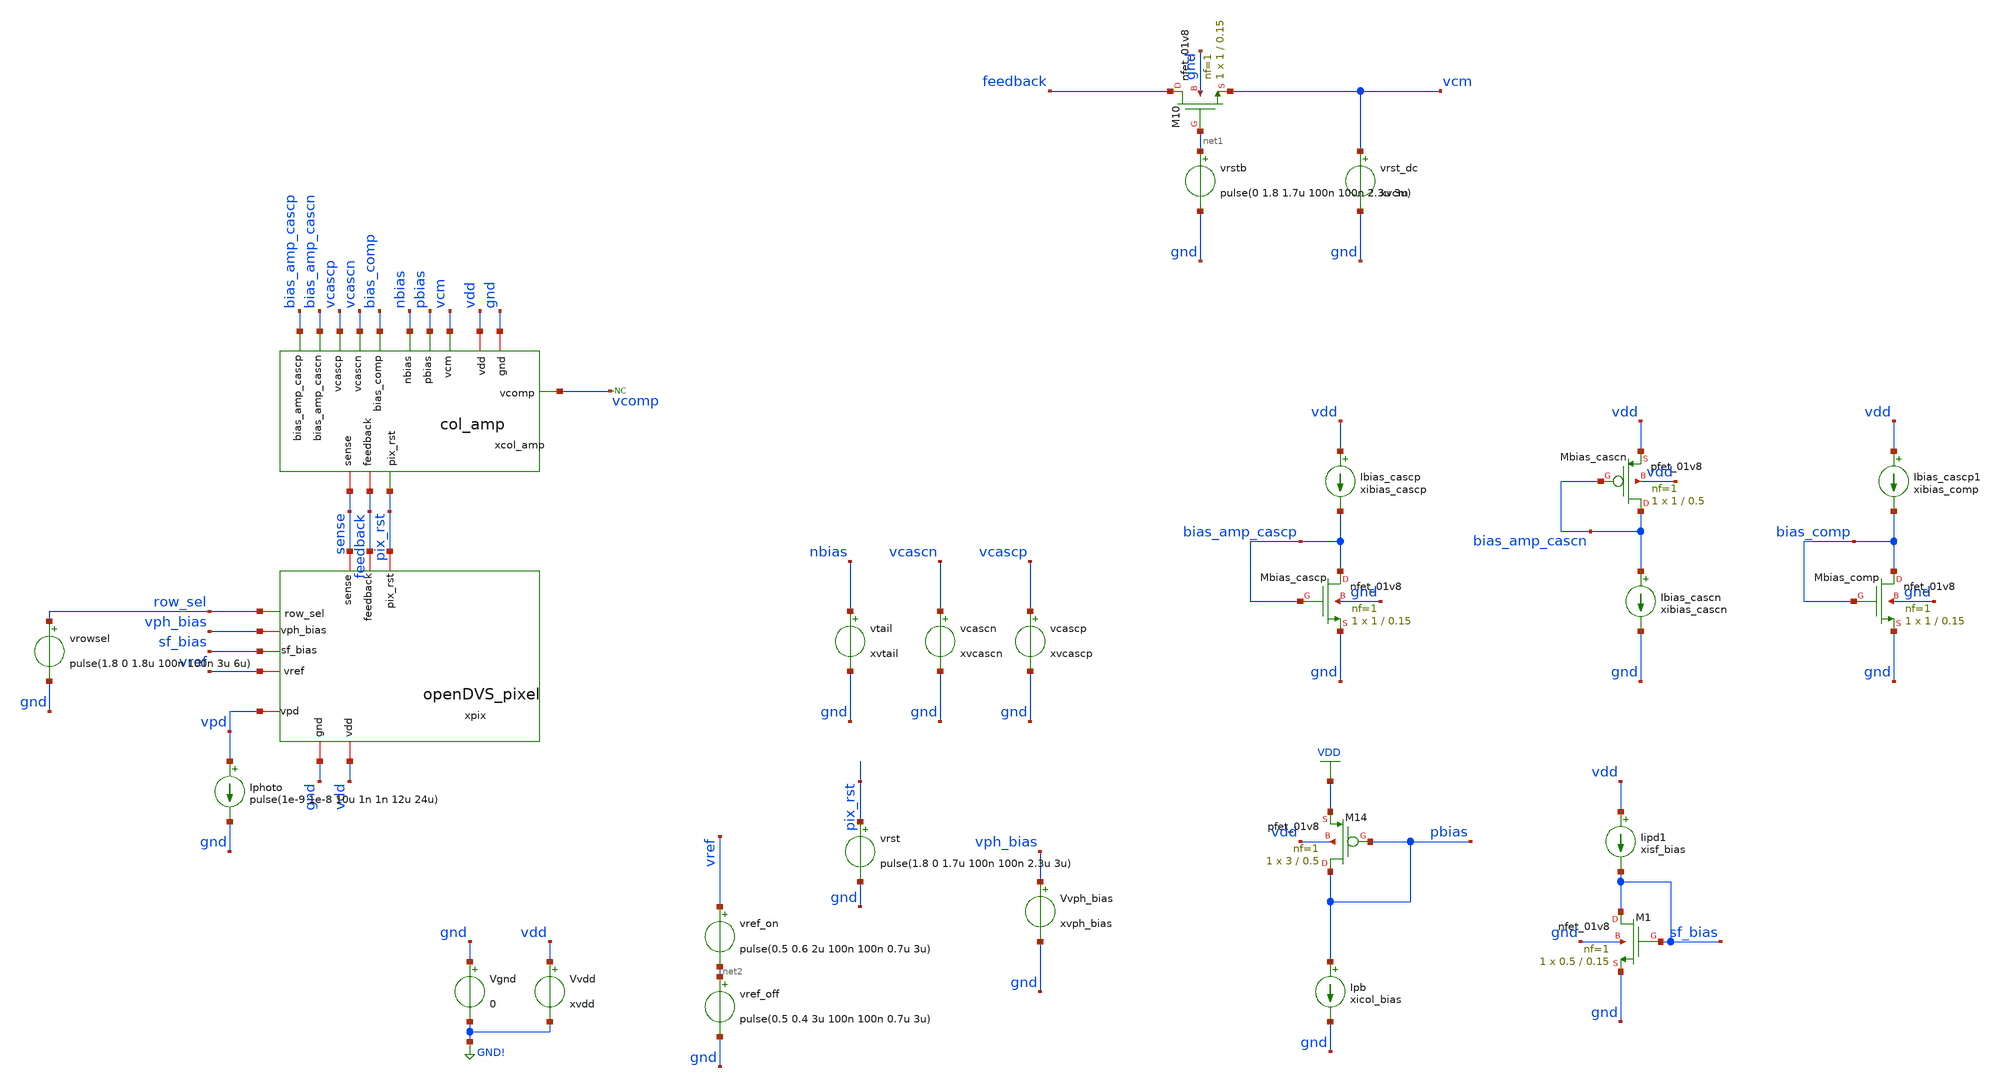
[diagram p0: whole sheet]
** sch_path: analog/xschem/1x1array_tb.sch
**.subckt 1x1array_tb
Ipb pbias gnd xicol_bias
XM14 pbias pbias VDD vdd sky130_fd_pr__pfet_01v8 L=0.5 W=3 nf=1 ad='int((1 + 1)/2) * 3 / 1 * 0.29' as='int((1 + 2)/2) * 3 / 1 * 0.29'
+ pd='2*int((1 + 1)/2) * (3 / 1 + 0.29)' ps='2*int((1 + 2)/2) * (3 / 1 + 0.29)' nrd='0.29 / 3 ' nrs='0.29 / 3 '
+ sa=0 sb=0 sd=0 mult=1 m=1
xcol_amp vdd pbias vcascp bias_amp_cascn vcm vcomp vcascn bias_comp pix_rst bias_amp_cascp gnd
+ feedback sense nbias col_amp
xpix feedback pix_rst sense row_sel vdd sf_bias gnd vref vpd vph_bias openDVS_pixel
XM1 sf_bias sf_bias gnd gnd sky130_fd_pr__nfet_01v8 L=0.15 W=0.5 nf=1 ad='int((1 + 1)/2) * 0.5 / 1 * 0.29'
+ as='int((1 + 2)/2) * 0.5 / 1 * 0.29' pd='2*int((1 + 1)/2) * (0.5 / 1 + 0.29)' ps='2*int((1 + 2)/2) * (0.5 / 1 + 0.29)'
+ nrd='0.29 / 0.5 ' nrs='0.29 / 0.5 ' sa=0 sb=0 sd=0 mult=1 m=1
Iipd1 vdd sf_bias xisf_bias
Vvph_bias vph_bias gnd xvph_bias
Vgnd gnd GND! 0
Vvdd vdd GND! xvdd
vtail nbias gnd xvtail
vcascn vcascn gnd xvcascn
vcascp vcascp gnd xvcascp
XMbias_cascp bias_amp_cascp bias_amp_cascp gnd gnd sky130_fd_pr__nfet_01v8 L=0.15 W=1 nf=1 ad='int((1 + 1)/2) * 1 / 1 * 0.29'
+ as='int((1 + 2)/2) * 1 / 1 * 0.29' pd='2*int((1 + 1)/2) * (1 / 1 + 0.29)' ps='2*int((1 + 2)/2) * (1 / 1 + 0.29)'
+ nrd='0.29 / 1 ' nrs='0.29 / 1 ' sa=0 sb=0 sd=0 mult=1 m=1
Ibias_cascp vdd bias_amp_cascp xibias_cascp
XMbias_cascn bias_amp_cascn bias_amp_cascn vdd vdd sky130_fd_pr__pfet_01v8 L=0.5 W=1 nf=1 ad='int((1 + 1)/2) * 1 / 1 * 0.29'
+ as='int((1 + 2)/2) * 1 / 1 * 0.29' pd='2*int((1 + 1)/2) * (1 / 1 + 0.29)' ps='2*int((1 + 2)/2) * (1 / 1 + 0.29)'
+ nrd='0.29 / 1 ' nrs='0.29 / 1 ' sa=0 sb=0 sd=0 mult=1 m=1
Ibias_cascn bias_amp_cascn gnd xibias_cascn
XM10 feedback net1 vcm gnd sky130_fd_pr__nfet_01v8 L=0.15 W=1 nf=1 ad='int((1 + 1)/2) * 1 / 1 * 0.29'
+ as='int((1 + 2)/2) * 1 / 1 * 0.29' pd='2*int((1 + 1)/2) * (1 / 1 + 0.29)' ps='2*int((1 + 2)/2) * (1 / 1 + 0.29)'
+ nrd='0.29 / 1 ' nrs='0.29 / 1 ' sa=0 sb=0 sd=0 mult=1 m=1
vrstb net1 gnd pulse(0 1.8 1.7u 100n 100n 2.3u 3u)
vrst_dc vcm gnd xvcm
Ibias_cascp1 vdd bias_comp xibias_comp
XMbias_comp bias_comp bias_comp gnd gnd sky130_fd_pr__nfet_01v8 L=0.15 W=1 nf=1 ad='int((1 + 1)/2) * 1 / 1 * 0.29'
+ as='int((1 + 2)/2) * 1 / 1 * 0.29' pd='2*int((1 + 1)/2) * (1 / 1 + 0.29)' ps='2*int((1 + 2)/2) * (1 / 1 + 0.29)'
+ nrd='0.29 / 1 ' nrs='0.29 / 1 ' sa=0 sb=0 sd=0 mult=1 m=1
vref_on vref net2 pulse(0.5 0.6 2u 100n 100n 0.7u 3u)
vref_off net2 gnd pulse(0.5 0.4 3u 100n 100n 0.7u 3u)
* noconn vcomp
Iphoto vpd gnd pulse(1e-9 1e-8 10u 1n 1n 12u 24u)
vrowsel row_sel gnd pulse(1.8 0 1.8u 100n 100n 3u 6u)
vrst pix_rst gnd pulse(1.8 0 1.7u 100n 100n 2.3u 3u)
**** begin user architecture code

** opencircuitdesign pdks install
.lib $::SKYWATER_MODELS/sky130.lib.spice tt


* sim
*.option reltol=1e-3 abstol=1e-12 vntol=1e-5 gmin=1e-10
*.option trtol=6 chgtol=1e-12

.control
.param xipd = 1e-9
.param xvph_bias = 1.5
.param xisf_bias = 9.2n
.param xvcascn = 0.2
.param xvcascp = 1.6
.param xicol_bias = 5e-7
.param xvtail = 0.5
.param xvcm = 0.6
.param xvdd = 1.8
.param xibias_cascp = 50n
.param xibias_cascn = 50n
.param xibias_comp = 50n
tran .1n 29u
* plot v(vref) v(sense) v(feedback) v(pix_rst)
save v(vref) v(sense) v(feedback) v(pix_rst)
save v(vcomp) v(xcol_amp.vout_sense)
*save i(xpix:vpd)

* save v(vphoto) v(vph_sf) v(vin) v(sense) v(feedback) v(vcomp)
* save v(pix_rst) v(vout) v(pbchk) v(vref) v(row_sel) v(lrst)
*ic v(vin)=0.6
*ic v(vout)=1
* dc vph 0 1.8 10m
*save all
* op
write 1x1array_tb.raw
.endc


**** end user architecture code
**.ends
.GLOBAL VDD
.GLOBAL GND!
.end
